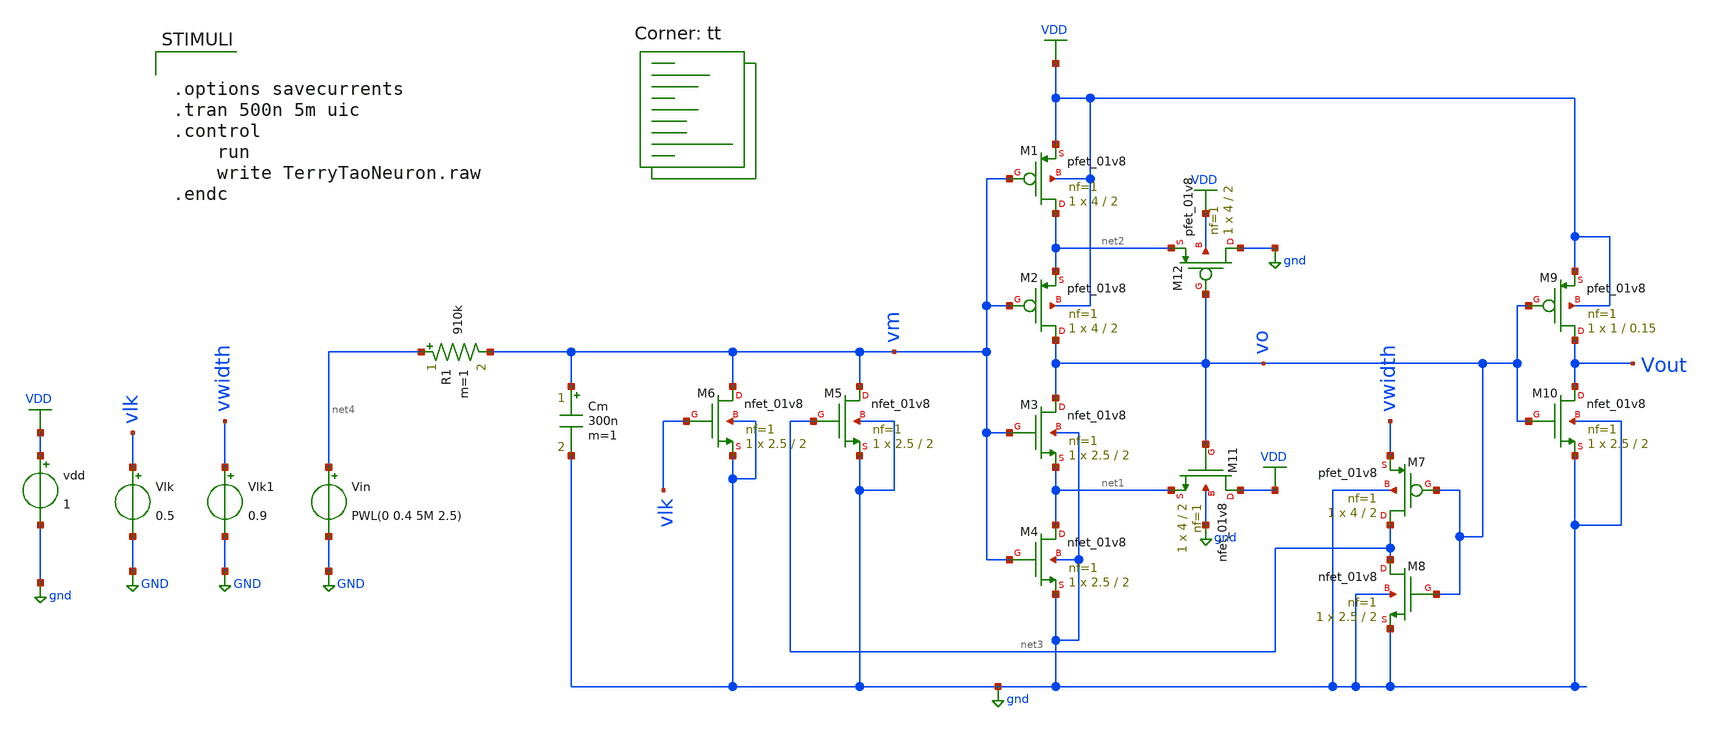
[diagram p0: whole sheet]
** sch_path: Neuron/TerryTaoNeuron/TerryTaoNeuron.sch
**.subckt TerryTaoNeuron
XM1 net2 vm VDD VDD sky130_fd_pr__pfet_01v8 L=2 W=4 nf=1 ad='int((nf+1)/2) * W/nf * 0.29' as='int((nf+2)/2) * W/nf * 0.29'
+ pd='2*int((nf+1)/2) * (W/nf + 0.29)' ps='2*int((nf+2)/2) * (W/nf + 0.29)' nrd='0.29 / W' nrs='0.29 / W'
+ sa=0 sb=0 sd=0 mult=1 m=1
XM2 vo vm net2 VDD sky130_fd_pr__pfet_01v8 L=2 W=4 nf=1 ad='int((nf+1)/2) * W/nf * 0.29' as='int((nf+2)/2) * W/nf * 0.29'
+ pd='2*int((nf+1)/2) * (W/nf + 0.29)' ps='2*int((nf+2)/2) * (W/nf + 0.29)' nrd='0.29 / W' nrs='0.29 / W'
+ sa=0 sb=0 sd=0 mult=1 m=1
XM3 vo vm net1 gnd sky130_fd_pr__nfet_01v8 L=2 W=2.5 nf=1 ad='int((1 + 1)/2) * 2.5 / 1 * 0.29' as='int((1 + 2)/2) * 2.5 / 1 * 0.29'
+ pd='2*int((1 + 1)/2) * (2.5 / 1 + 0.29)' ps='2*int((1 + 2)/2) * (2.5 / 1 + 0.29)' nrd='0.29 / 2.5 ' nrs='0.29 / 2.5 '
+ sa=0 sb=0 sd=0 mult=1 m=1
XM4 net1 vm gnd gnd sky130_fd_pr__nfet_01v8 L=2 W=2.5 nf=1 ad='int((1 + 1)/2) * 2.5 / 1 * 0.29' as='int((1 + 2)/2) * 2.5 / 1 * 0.29'
+ pd='2*int((1 + 1)/2) * (2.5 / 1 + 0.29)' ps='2*int((1 + 2)/2) * (2.5 / 1 + 0.29)' nrd='0.29 / 2.5 ' nrs='0.29 / 2.5 '
+ sa=0 sb=0 sd=0 mult=1 m=1
XM5 vm net3 gnd gnd sky130_fd_pr__nfet_01v8 L=2 W=2.5 nf=1 ad='int((1 + 1)/2) * 2.5 / 1 * 0.29' as='int((1 + 2)/2) * 2.5 / 1 * 0.29'
+ pd='2*int((1 + 1)/2) * (2.5 / 1 + 0.29)' ps='2*int((1 + 2)/2) * (2.5 / 1 + 0.29)' nrd='0.29 / 2.5 ' nrs='0.29 / 2.5 '
+ sa=0 sb=0 sd=0 mult=1 m=1
XM6 vm vlk gnd gnd sky130_fd_pr__nfet_01v8 L=2 W=2.5 nf=1 ad='int((1 + 1)/2) * 2.5 / 1 * 0.29' as='int((1 + 2)/2) * 2.5 / 1 * 0.29'
+ pd='2*int((1 + 1)/2) * (2.5 / 1 + 0.29)' ps='2*int((1 + 2)/2) * (2.5 / 1 + 0.29)' nrd='0.29 / 2.5 ' nrs='0.29 / 2.5 '
+ sa=0 sb=0 sd=0 mult=1 m=1
Cm vm gnd 300n m=1
Vlk vlk GND 0.5
XM7 net3 vo vwidth gnd sky130_fd_pr__pfet_01v8 L=2 W=4 nf=1 ad='int((nf+1)/2) * W/nf * 0.29' as='int((nf+2)/2) * W/nf * 0.29'
+ pd='2*int((nf+1)/2) * (W/nf + 0.29)' ps='2*int((nf+2)/2) * (W/nf + 0.29)' nrd='0.29 / W' nrs='0.29 / W'
+ sa=0 sb=0 sd=0 mult=1 m=1
XM8 net3 vo gnd gnd sky130_fd_pr__nfet_01v8 L=2 W=2.5 nf=1 ad='int((1 + 1)/2) * 2.5 / 1 * 0.29' as='int((1 + 2)/2) * 2.5 / 1 * 0.29'
+ pd='2*int((1 + 1)/2) * (2.5 / 1 + 0.29)' ps='2*int((1 + 2)/2) * (2.5 / 1 + 0.29)' nrd='0.29 / 2.5 ' nrs='0.29 / 2.5 '
+ sa=0 sb=0 sd=0 mult=1 m=1
XM9 Vout vo VDD VDD sky130_fd_pr__pfet_01v8 L=0.15 W=1 nf=1 ad='int((nf+1)/2) * W/nf * 0.29' as='int((nf+2)/2) * W/nf * 0.29'
+ pd='2*int((nf+1)/2) * (W/nf + 0.29)' ps='2*int((nf+2)/2) * (W/nf + 0.29)' nrd='0.29 / W' nrs='0.29 / W'
+ sa=0 sb=0 sd=0 mult=1 m=1
XM11 VDD vo net1 gnd sky130_fd_pr__nfet_01v8 L=2 W=4 nf=1 ad='int((1 + 1)/2) * 4 / 1 * 0.29' as='int((1 + 2)/2) * 4 / 1 * 0.29'
+ pd='2*int((1 + 1)/2) * (4 / 1 + 0.29)' ps='2*int((1 + 2)/2) * (4 / 1 + 0.29)' nrd='0.29 / 4 ' nrs='0.29 / 4 '
+ sa=0 sb=0 sd=0 mult=1 m=1
XM12 gnd vo net2 VDD sky130_fd_pr__pfet_01v8 L=2 W=4 nf=1 ad='int((nf+1)/2) * W/nf * 0.29' as='int((nf+2)/2) * W/nf * 0.29'
+ pd='2*int((nf+1)/2) * (W/nf + 0.29)' ps='2*int((nf+2)/2) * (W/nf + 0.29)' nrd='0.29 / W' nrs='0.29 / W'
+ sa=0 sb=0 sd=0 mult=1 m=1
vdd VDD gnd 1
XM10 Vout vo gnd gnd sky130_fd_pr__nfet_01v8 L=2 W=2.5 nf=1 ad='int((1 + 1)/2) * 2.5 / 1 * 0.29' as='int((1 + 2)/2) * 2.5 / 1 * 0.29'
+ pd='2*int((1 + 1)/2) * (2.5 / 1 + 0.29)' ps='2*int((1 + 2)/2) * (2.5 / 1 + 0.29)' nrd='0.29 / 2.5 ' nrs='0.29 / 2.5 '
+ sa=0 sb=0 sd=0 mult=1 m=1
Vlk1 vwidth GND 0.9
R1 net4 vm 910k m=1
Vin net4 GND PWL(0 0.4 5M 2.5)
**** begin user architecture code
.lib $::SKYWATER_MODELS/sky130.lib.spice tt
**** end user architecture code
**.ends
.GLOBAL GND
.GLOBAL VDD
.GLOBAL gnd
**** begin user architecture code


.options savecurrents
.tran 500n 5m uic
.control
	run
	write TerryTaoNeuron.raw
.endc


**** end user architecture code
.end
